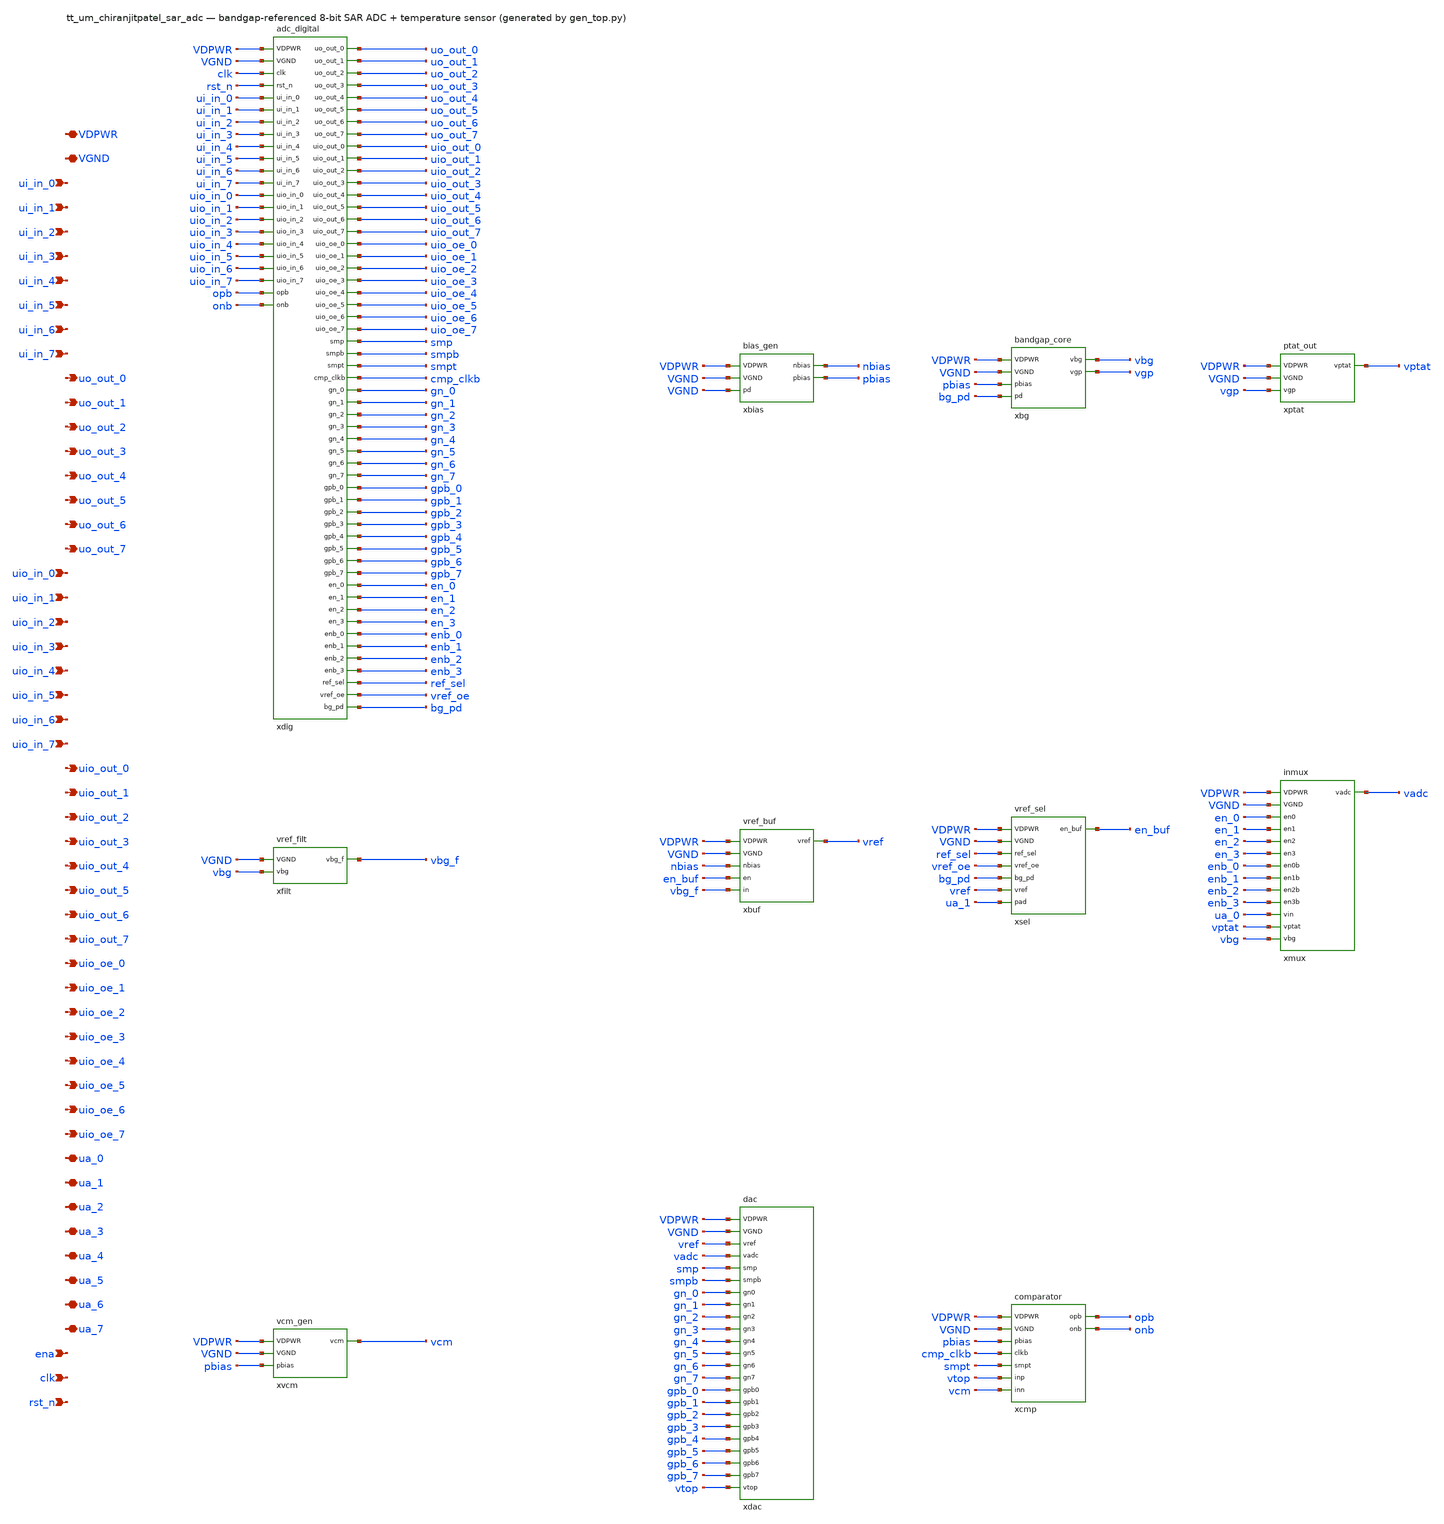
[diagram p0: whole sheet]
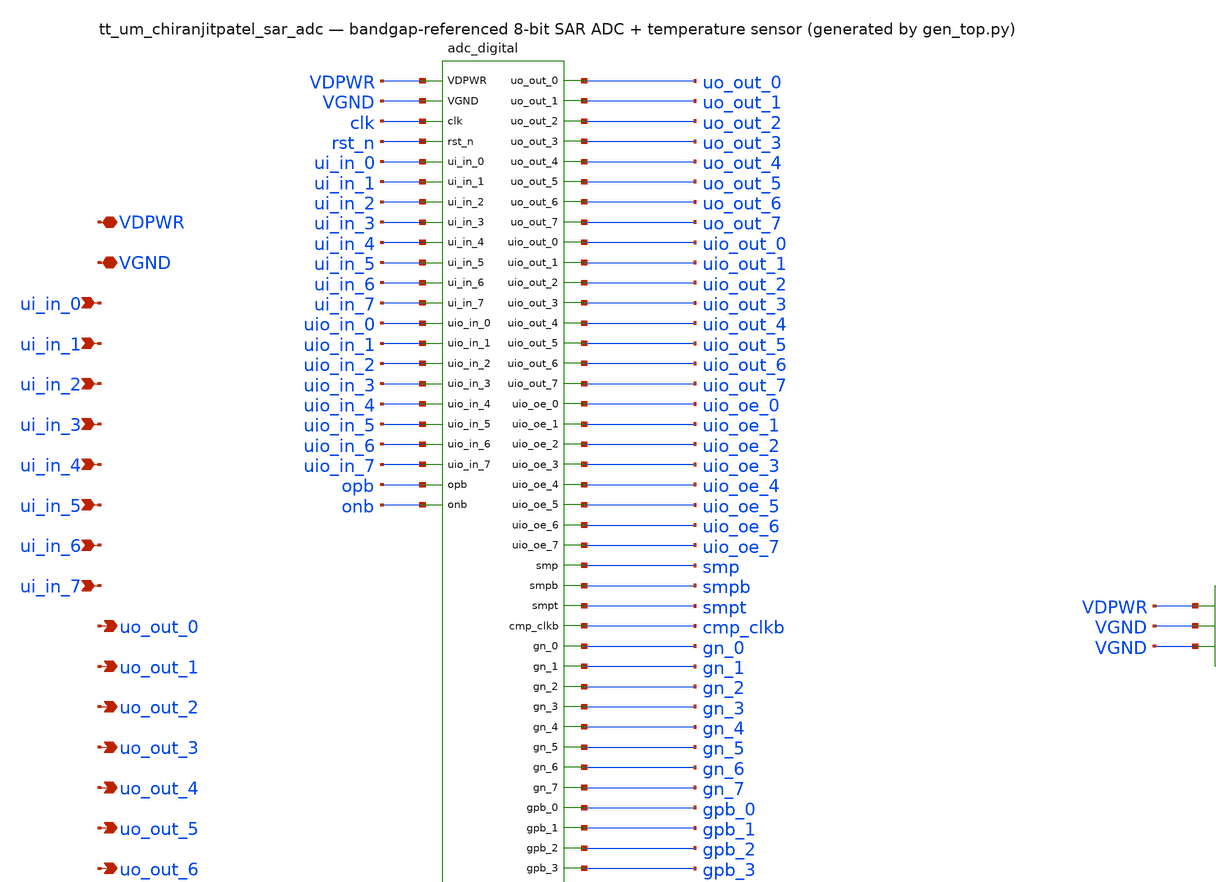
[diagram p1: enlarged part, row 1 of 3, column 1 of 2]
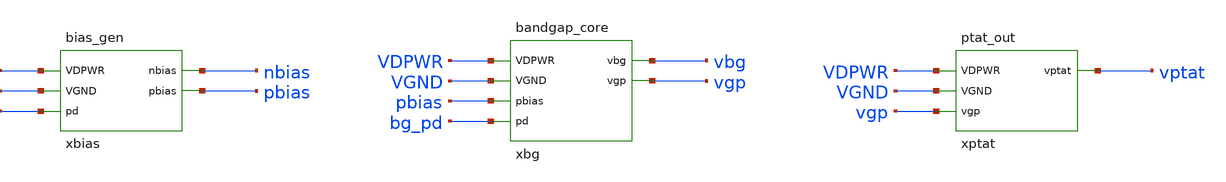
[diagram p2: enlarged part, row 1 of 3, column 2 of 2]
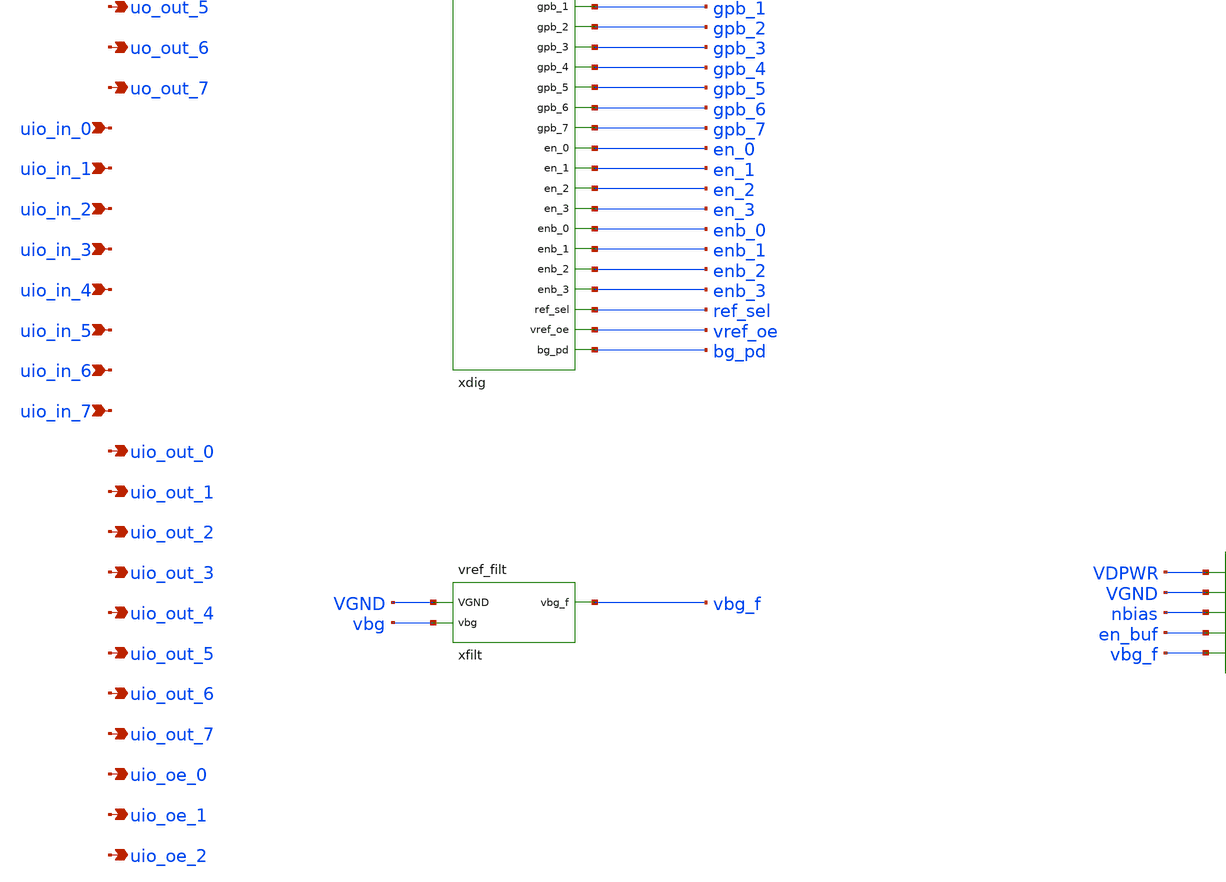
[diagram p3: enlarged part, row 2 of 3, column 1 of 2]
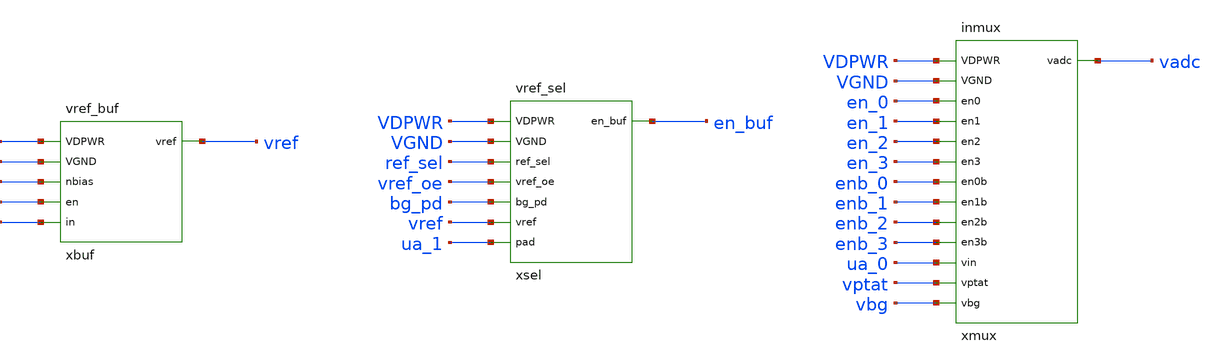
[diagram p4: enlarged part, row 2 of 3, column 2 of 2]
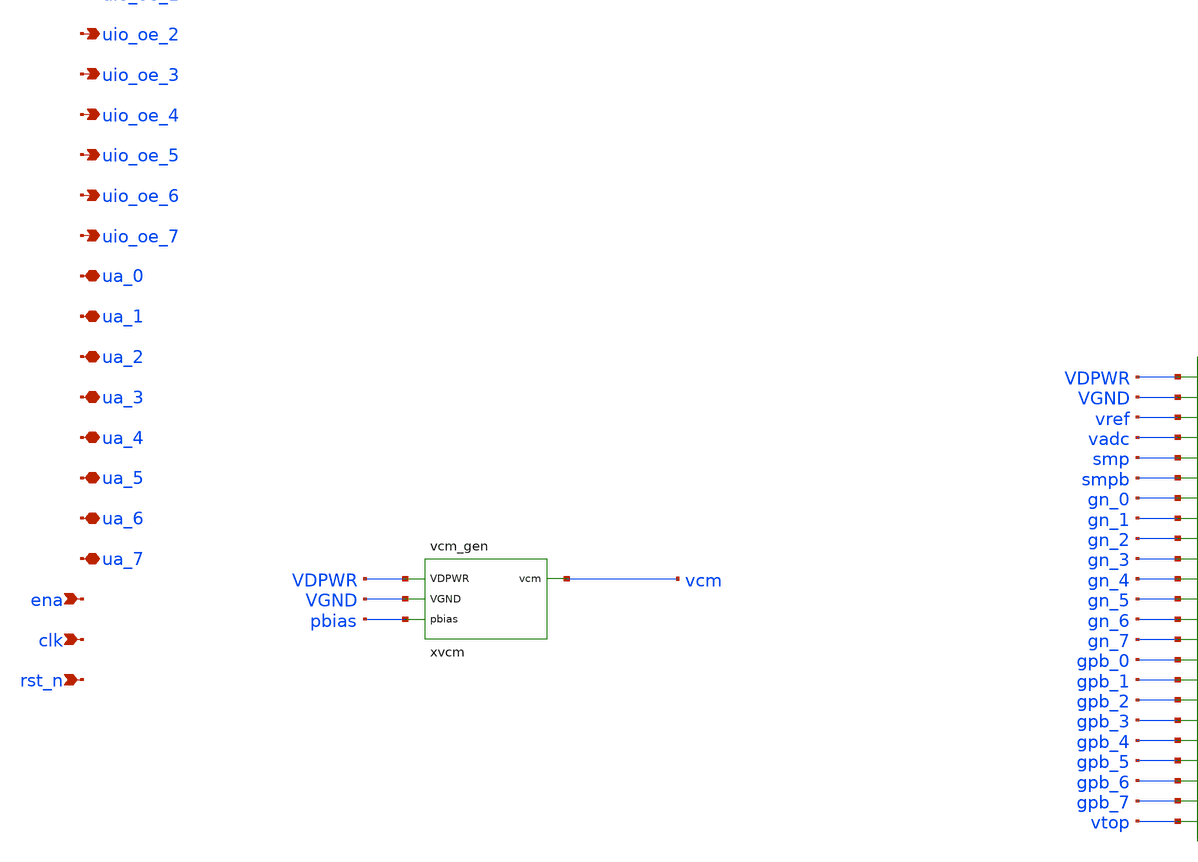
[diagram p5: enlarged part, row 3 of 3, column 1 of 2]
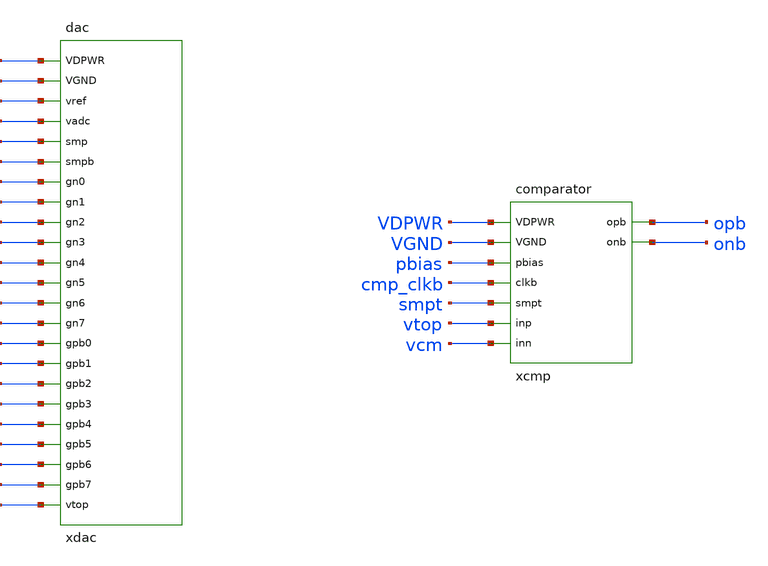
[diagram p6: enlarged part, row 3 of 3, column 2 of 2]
** sch_path: xschem/tt_um_chiranjitpatel_sar_adc.sch
**.subckt tt_um_chiranjitpatel_sar_adc VDPWR VGND ui_in_0 ui_in_1 ui_in_2 ui_in_3 ui_in_4 ui_in_5
*+ ui_in_6 ui_in_7 uo_out_0 uo_out_1 uo_out_2 uo_out_3 uo_out_4 uo_out_5 uo_out_6 uo_out_7 uio_in_0 uio_in_1
*+ uio_in_2 uio_in_3 uio_in_4 uio_in_5 uio_in_6 uio_in_7 uio_out_0 uio_out_1 uio_out_2 uio_out_3 uio_out_4
*+ uio_out_5 uio_out_6 uio_out_7 uio_oe_0 uio_oe_1 uio_oe_2 uio_oe_3 uio_oe_4 uio_oe_5 uio_oe_6 uio_oe_7 ua_0
*+ ua_1 ua_2 ua_3 ua_4 ua_5 ua_6 ua_7 ena clk rst_n
*.iopin VDPWR
*.iopin VGND
*.ipin ui_in_0
*.ipin ui_in_1
*.ipin ui_in_2
*.ipin ui_in_3
*.ipin ui_in_4
*.ipin ui_in_5
*.ipin ui_in_6
*.ipin ui_in_7
*.opin uo_out_0
*.opin uo_out_1
*.opin uo_out_2
*.opin uo_out_3
*.opin uo_out_4
*.opin uo_out_5
*.opin uo_out_6
*.opin uo_out_7
*.ipin uio_in_0
*.ipin uio_in_1
*.ipin uio_in_2
*.ipin uio_in_3
*.ipin uio_in_4
*.ipin uio_in_5
*.ipin uio_in_6
*.ipin uio_in_7
*.opin uio_out_0
*.opin uio_out_1
*.opin uio_out_2
*.opin uio_out_3
*.opin uio_out_4
*.opin uio_out_5
*.opin uio_out_6
*.opin uio_out_7
*.opin uio_oe_0
*.opin uio_oe_1
*.opin uio_oe_2
*.opin uio_oe_3
*.opin uio_oe_4
*.opin uio_oe_5
*.opin uio_oe_6
*.opin uio_oe_7
*.iopin ua_0
*.iopin ua_1
*.iopin ua_2
*.iopin ua_3
*.iopin ua_4
*.iopin ua_5
*.iopin ua_6
*.iopin ua_7
*.ipin ena
*.ipin clk
*.ipin rst_n
xdig VDPWR VGND clk rst_n ui_in_0 ui_in_1 ui_in_2 ui_in_3 ui_in_4 ui_in_5 ui_in_6 ui_in_7 uio_in_0
+ uio_in_1 uio_in_2 uio_in_3 uio_in_4 uio_in_5 uio_in_6 uio_in_7 opb onb uo_out_0 uo_out_1 uo_out_2 uo_out_3
+ uo_out_4 uo_out_5 uo_out_6 uo_out_7 uio_out_0 uio_out_1 uio_out_2 uio_out_3 uio_out_4 uio_out_5 uio_out_6
+ uio_out_7 uio_oe_0 uio_oe_1 uio_oe_2 uio_oe_3 uio_oe_4 uio_oe_5 uio_oe_6 uio_oe_7 smp smpb smpt cmp_clkb gn_0
+ gn_1 gn_2 gn_3 gn_4 gn_5 gn_6 gn_7 gpb_0 gpb_1 gpb_2 gpb_3 gpb_4 gpb_5 gpb_6 gpb_7 en_0 en_1 en_2 en_3
+ enb_0 enb_1 enb_2 enb_3 ref_sel vref_oe bg_pd adc_digital
xbias VDPWR VGND VGND nbias pbias bias_gen
xbg VDPWR VGND pbias bg_pd vbg vgp bandgap_core
xptat VDPWR VGND vgp vptat ptat_out
xfilt VGND vbg vbg_f vref_filt
xbuf VDPWR VGND nbias en_buf vbg_f vref vref_buf
xsel VDPWR VGND ref_sel vref_oe bg_pd vref ua_1 en_buf vref_sel
xmux VDPWR VGND en_0 en_1 en_2 en_3 enb_0 enb_1 enb_2 enb_3 ua_0 vptat vbg vadc inmux
xvcm VDPWR VGND pbias vcm vcm_gen
xdac VDPWR VGND vref vadc smp smpb gn_0 gn_1 gn_2 gn_3 gn_4 gn_5 gn_6 gn_7 gpb_0 gpb_1 gpb_2 gpb_3
+ gpb_4 gpb_5 gpb_6 gpb_7 vtop dac
xcmp VDPWR VGND pbias cmp_clkb smpt vtop vcm opb onb comparator
**.ends
.end
